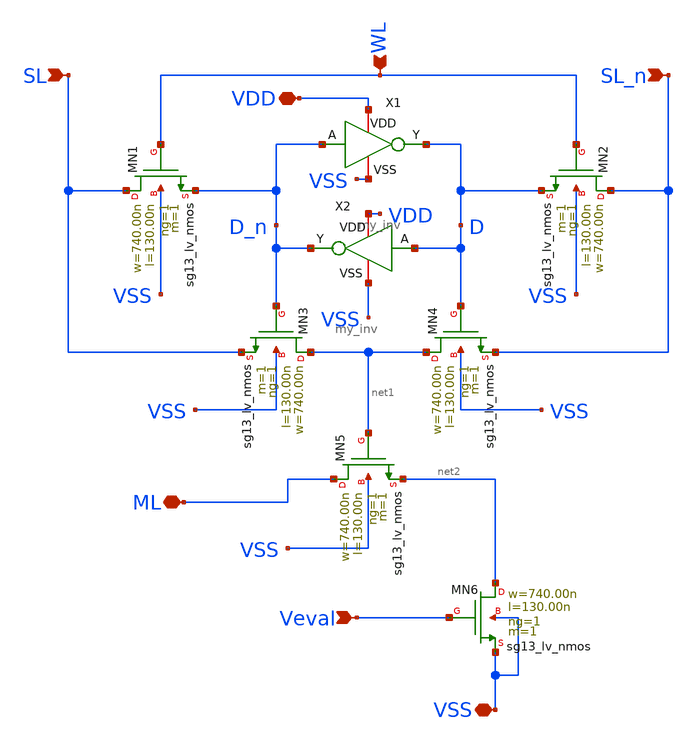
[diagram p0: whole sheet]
** sch_path: xschem/bitcell.sch
**.subckt bitcell SL SL_n WL ML Veval VDD VSS
*.ipin SL
*.ipin SL_n
*.ipin WL
*.iopin ML
*.ipin Veval
*.iopin VDD
*.iopin VSS
XMN1 SL WL D_n VSS sg13_lv_nmos w=740.00n l=130.00n ng=1 m=1 mm_ok=1
XMN2 SL_n WL D VSS sg13_lv_nmos w=740.00n l=130.00n ng=1 m=1 mm_ok=1
XMN3 net1 D_n SL VSS sg13_lv_nmos w=740.00n l=130.00n ng=1 m=1 mm_ok=1
XMN4 net1 D SL_n VSS sg13_lv_nmos w=740.00n l=130.00n ng=1 m=1 mm_ok=1
XMN5 ML net1 net2 VSS sg13_lv_nmos w=740.00n l=130.00n ng=1 m=1 mm_ok=1
XMN6 net2 Veval VSS VSS sg13_lv_nmos w=740.00n l=130.00n ng=1 m=1 mm_ok=1
X1 VDD D D_n VSS my_inv
X2 VDD D_n D VSS my_inv
**.ends

* expanding   symbol:  /home/designer/shared/my_inv.sym # of pins=4
** sym_path: xschem/my_inv.sym
** sch_path: xschem/my_inv.sch
.subckt my_inv VDD Y A VSS
*.opin Y
*.ipin A
*.iopin VDD
*.iopin VSS
XMN0 Y A VSS VSS sg13_lv_nmos w=740.00n l=130.00n ng=1 m=1 mm_ok=1
XMP0 Y A VDD VDD sg13_lv_pmos w=1.12u l=130.00n ng=1 m=1 mm_ok=1
.ends

.end
